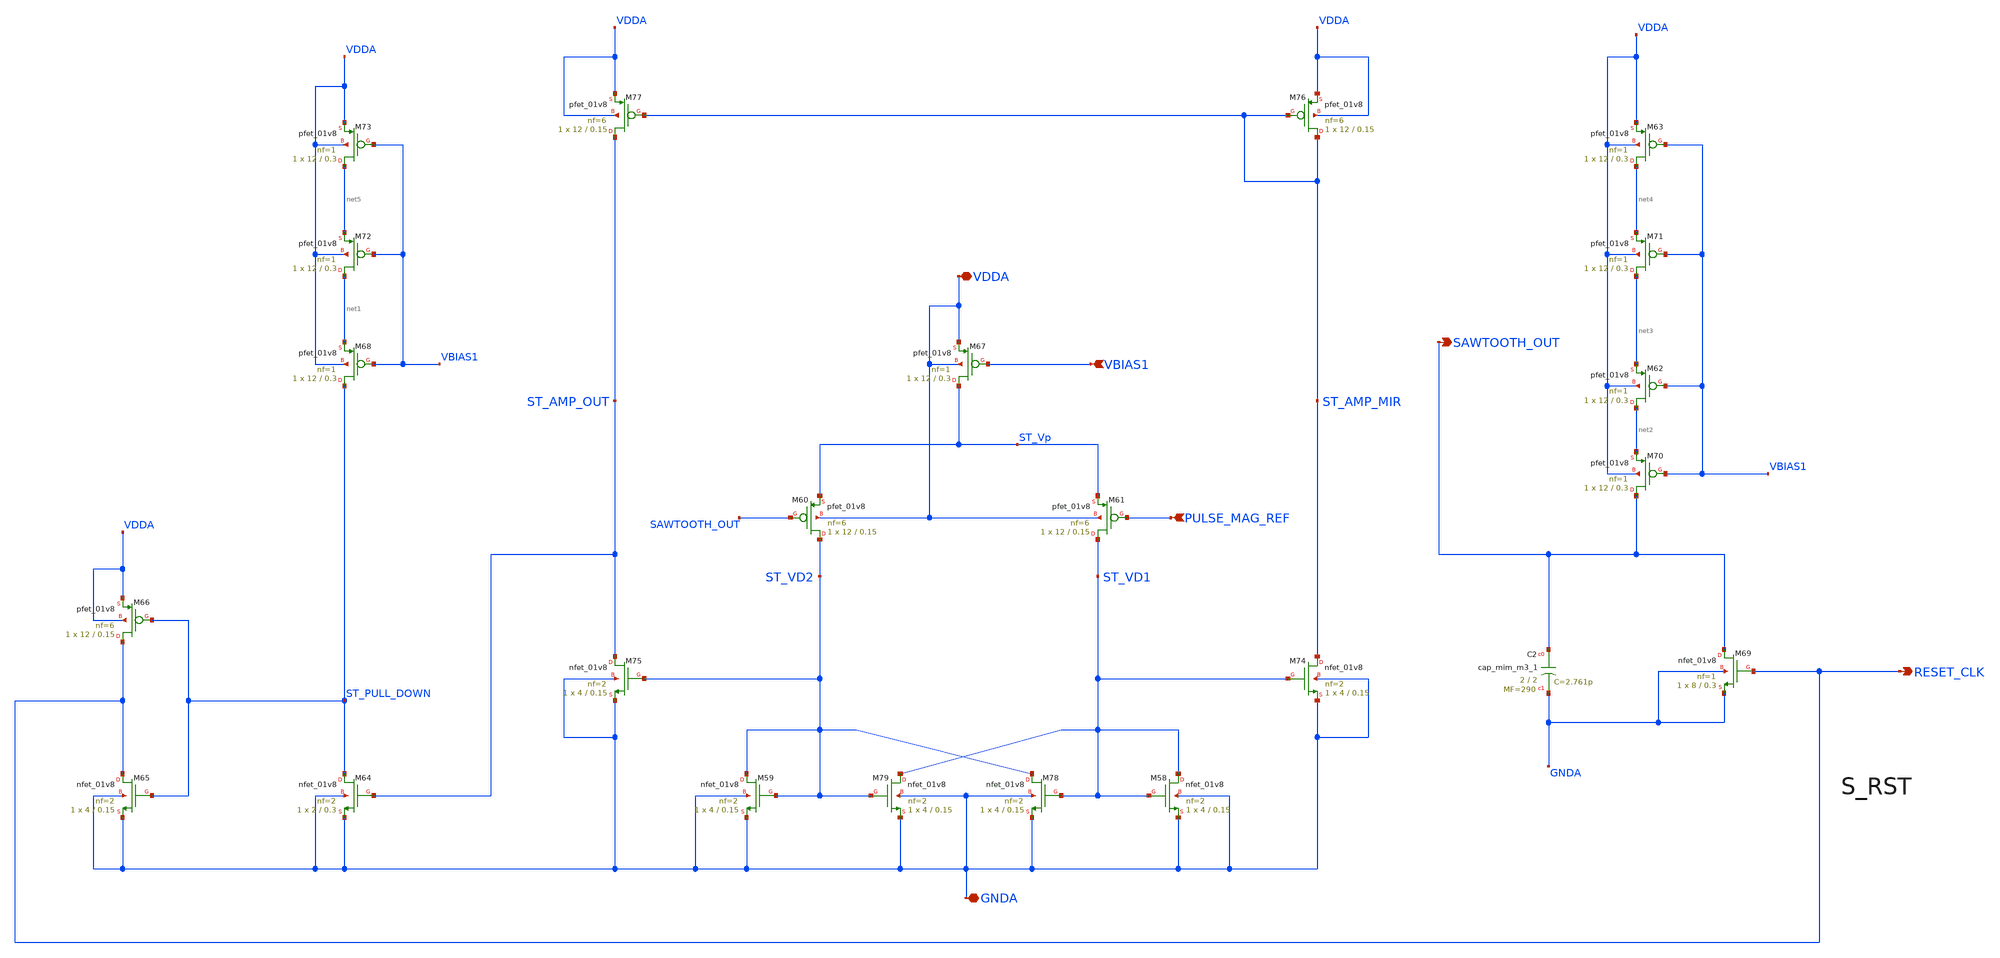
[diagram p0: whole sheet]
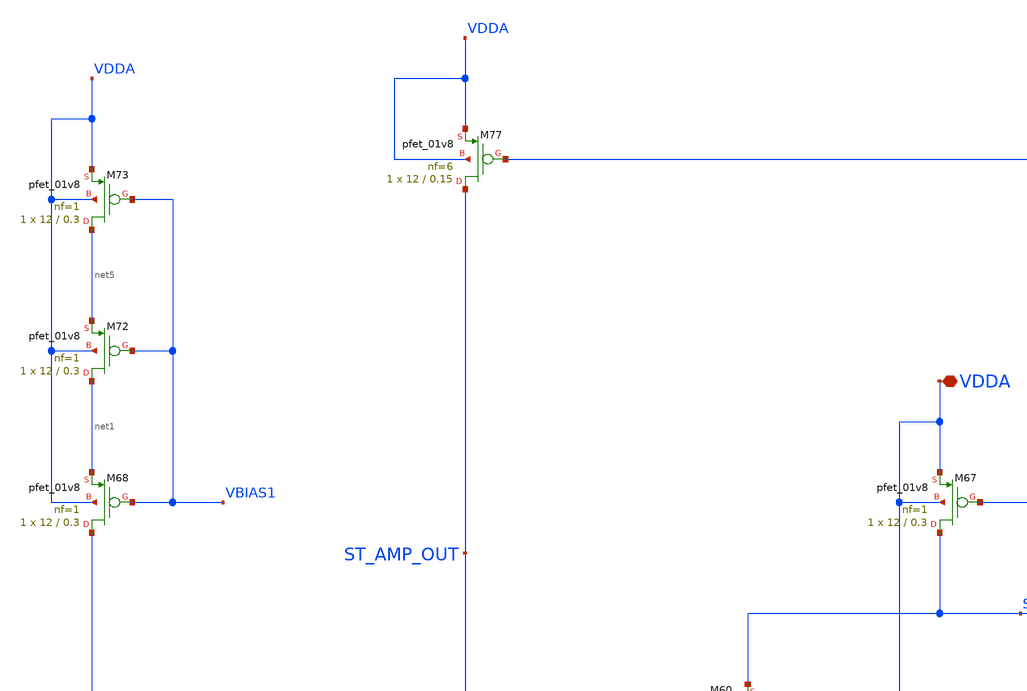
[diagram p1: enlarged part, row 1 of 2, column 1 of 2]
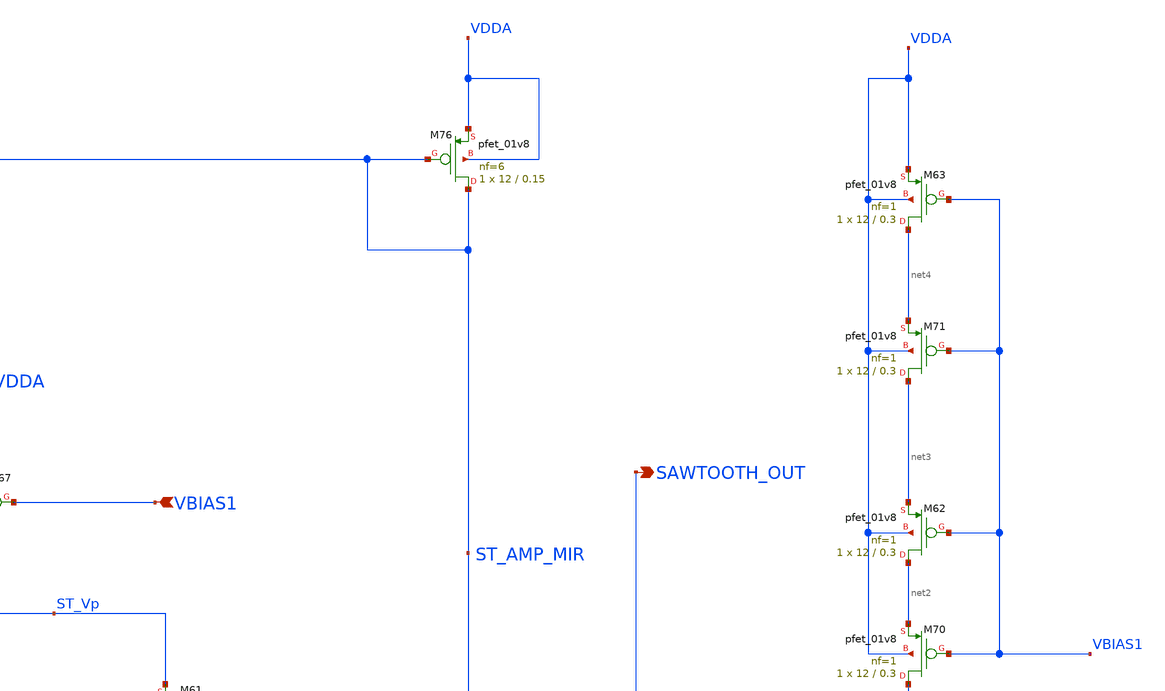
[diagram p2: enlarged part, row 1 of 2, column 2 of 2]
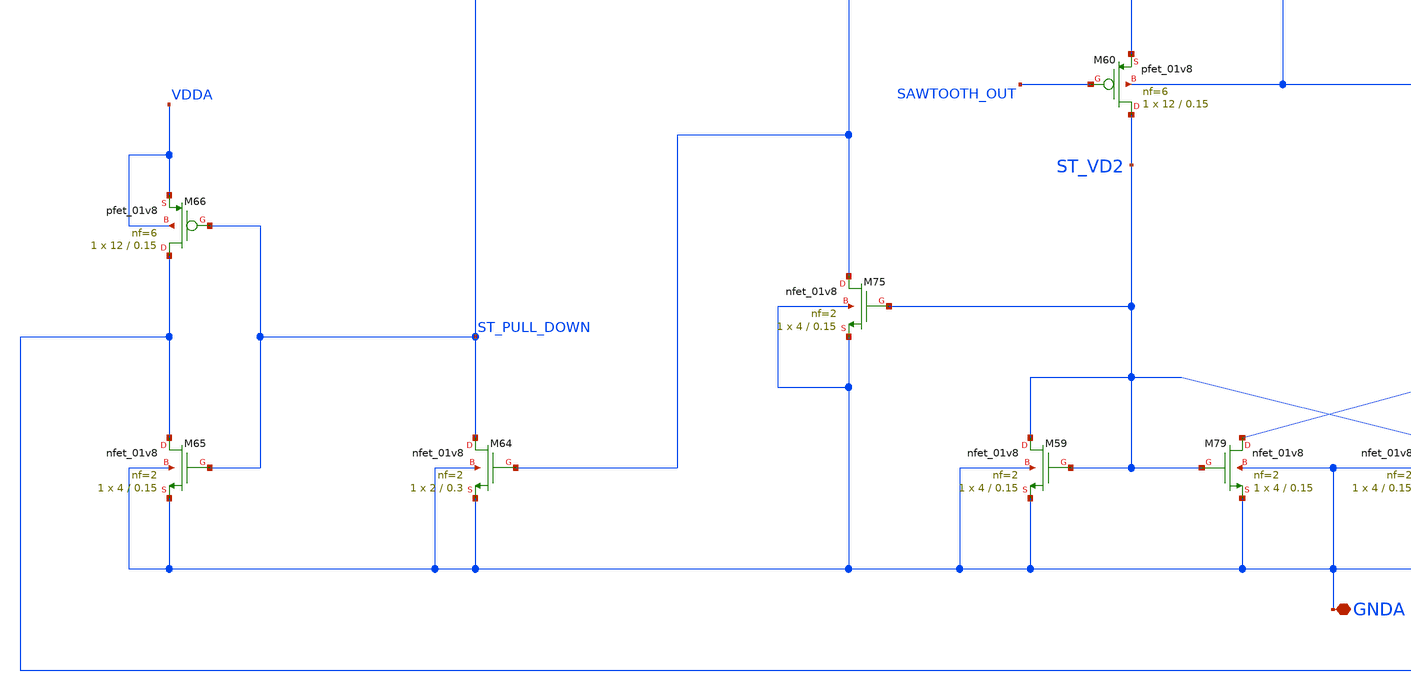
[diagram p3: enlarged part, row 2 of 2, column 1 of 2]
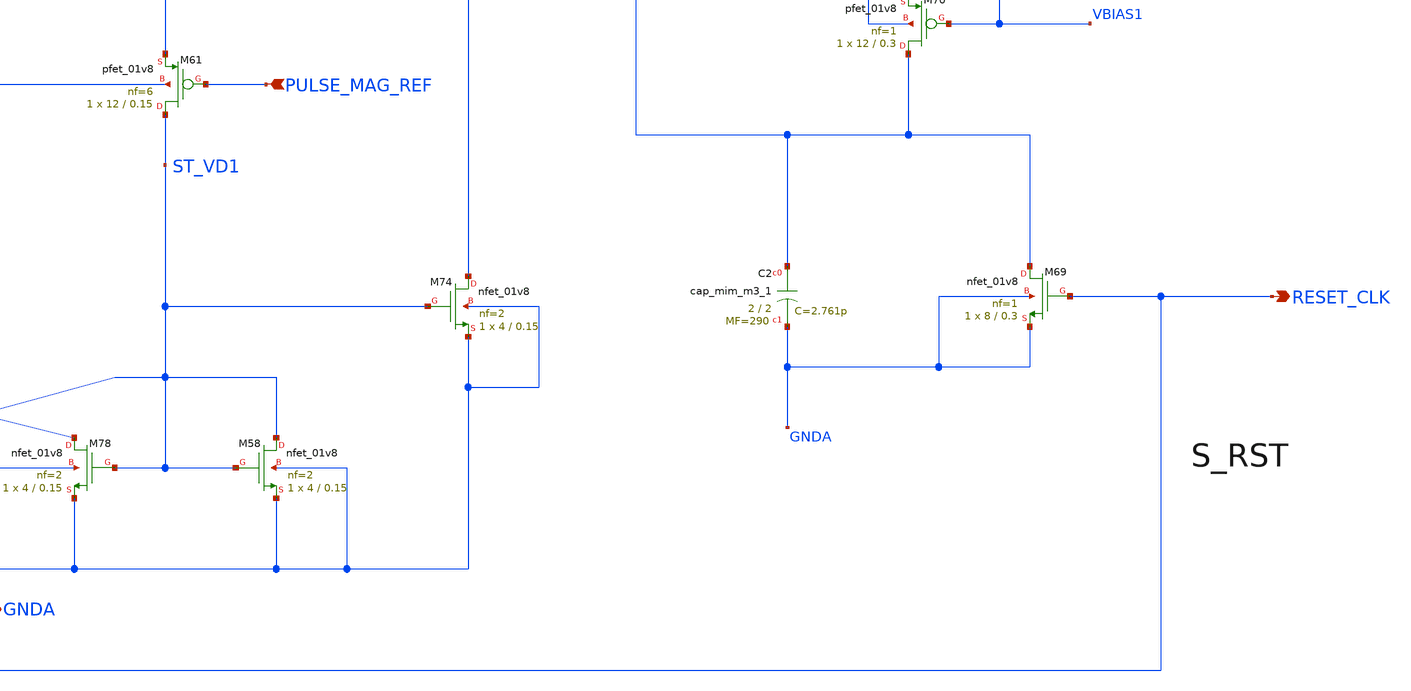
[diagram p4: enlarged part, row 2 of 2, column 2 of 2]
** sch_path: projects/ASU/EEE572/schematic/sawtooth_generator.sch
**.subckt sawtooth_generator VBIAS1 VDDA GNDA PULSE_MAG_REF SAWTOOTH_OUT RESET_CLK
*.ipin VBIAS1
*.iopin VDDA
*.iopin GNDA
*.ipin PULSE_MAG_REF
*.opin SAWTOOTH_OUT
*.opin RESET_CLK
XM58 ST_VD1 ST_VD1 GNDA GNDA sky130_fd_pr__nfet_01v8 L=0.15 W=4 nf=2 ad='int((nf+1)/2) * W/nf * 0.29'
+ as='int((nf+2)/2) * W/nf * 0.29' pd='2*int((nf+1)/2) * (W/nf + 0.29)' ps='2*int((nf+2)/2) * (W/nf + 0.29)'
+ nrd='0.29 / W' nrs='0.29 / W' sa=0 sb=0 sd=0 mult=1 m=1
XM59 ST_VD2 ST_VD2 GNDA GNDA sky130_fd_pr__nfet_01v8 L=0.15 W=4 nf=2 ad='int((nf+1)/2) * W/nf * 0.29'
+ as='int((nf+2)/2) * W/nf * 0.29' pd='2*int((nf+1)/2) * (W/nf + 0.29)' ps='2*int((nf+2)/2) * (W/nf + 0.29)'
+ nrd='0.29 / W' nrs='0.29 / W' sa=0 sb=0 sd=0 mult=1 m=1
XM60 ST_VD2 SAWTOOTH_OUT ST_Vp VDDA sky130_fd_pr__pfet_01v8 L=0.15 W=12 nf=6 ad='int((nf+1)/2) * W/nf * 0.29'
+ as='int((nf+2)/2) * W/nf * 0.29' pd='2*int((nf+1)/2) * (W/nf + 0.29)' ps='2*int((nf+2)/2) * (W/nf + 0.29)'
+ nrd='0.29 / W' nrs='0.29 / W' sa=0 sb=0 sd=0 mult=1 m=1
XM61 ST_VD1 PULSE_MAG_REF ST_Vp VDDA sky130_fd_pr__pfet_01v8 L=0.15 W=12 nf=6 ad='int((nf+1)/2) * W/nf * 0.29'
+ as='int((nf+2)/2) * W/nf * 0.29' pd='2*int((nf+1)/2) * (W/nf + 0.29)' ps='2*int((nf+2)/2) * (W/nf + 0.29)'
+ nrd='0.29 / W' nrs='0.29 / W' sa=0 sb=0 sd=0 mult=1 m=1
XM64 ST_PULL_DOWN ST_AMP_OUT GNDA GNDA sky130_fd_pr__nfet_01v8 L=0.3 W=2 nf=2 ad='int((nf+1)/2) * W/nf * 0.29'
+ as='int((nf+2)/2) * W/nf * 0.29' pd='2*int((nf+1)/2) * (W/nf + 0.29)' ps='2*int((nf+2)/2) * (W/nf + 0.29)'
+ nrd='0.29 / W' nrs='0.29 / W' sa=0 sb=0 sd=0 mult=1 m=1
XM65 RESET_CLK ST_PULL_DOWN GNDA GNDA sky130_fd_pr__nfet_01v8 L=0.15 W=4 nf=2 ad='int((nf+1)/2) * W/nf * 0.29'
+ as='int((nf+2)/2) * W/nf * 0.29' pd='2*int((nf+1)/2) * (W/nf + 0.29)' ps='2*int((nf+2)/2) * (W/nf + 0.29)'
+ nrd='0.29 / W' nrs='0.29 / W' sa=0 sb=0 sd=0 mult=1 m=1
XM66 RESET_CLK ST_PULL_DOWN VDDA VDDA sky130_fd_pr__pfet_01v8 L=0.15 W=12 nf=6 ad='int((nf+1)/2) * W/nf * 0.29'
+ as='int((nf+2)/2) * W/nf * 0.29' pd='2*int((nf+1)/2) * (W/nf + 0.29)' ps='2*int((nf+2)/2) * (W/nf + 0.29)'
+ nrd='0.29 / W' nrs='0.29 / W' sa=0 sb=0 sd=0 mult=1 m=1
XM67 ST_Vp VBIAS1 VDDA VDDA sky130_fd_pr__pfet_01v8 L=0.3 W=12 nf=1 ad='int((nf+1)/2) * W/nf * 0.29'
+ as='int((nf+2)/2) * W/nf * 0.29' pd='2*int((nf+1)/2) * (W/nf + 0.29)' ps='2*int((nf+2)/2) * (W/nf + 0.29)'
+ nrd='0.29 / W' nrs='0.29 / W' sa=0 sb=0 sd=0 mult=1 m=1
XM68 ST_PULL_DOWN VBIAS1 net1 VDDA sky130_fd_pr__pfet_01v8 L=0.3 W=12 nf=1 ad='int((nf+1)/2) * W/nf * 0.29'
+ as='int((nf+2)/2) * W/nf * 0.29' pd='2*int((nf+1)/2) * (W/nf + 0.29)' ps='2*int((nf+2)/2) * (W/nf + 0.29)'
+ nrd='0.29 / W' nrs='0.29 / W' sa=0 sb=0 sd=0 mult=1 m=1
XC2 SAWTOOTH_OUT GNDA sky130_fd_pr__cap_mim_m3_1 W=2 L=2 MF=290 m=290
XM69 SAWTOOTH_OUT RESET_CLK GNDA GNDA sky130_fd_pr__nfet_01v8 L=0.3 W=8 nf=1 ad='int((nf+1)/2) * W/nf * 0.29'
+ as='int((nf+2)/2) * W/nf * 0.29' pd='2*int((nf+1)/2) * (W/nf + 0.29)' ps='2*int((nf+2)/2) * (W/nf + 0.29)'
+ nrd='0.29 / W' nrs='0.29 / W' sa=0 sb=0 sd=0 mult=1 m=1
XM70 SAWTOOTH_OUT VBIAS1 net2 VDDA sky130_fd_pr__pfet_01v8 L=0.3 W=12 nf=1 ad='int((nf+1)/2) * W/nf * 0.29'
+ as='int((nf+2)/2) * W/nf * 0.29' pd='2*int((nf+1)/2) * (W/nf + 0.29)' ps='2*int((nf+2)/2) * (W/nf + 0.29)'
+ nrd='0.29 / W' nrs='0.29 / W' sa=0 sb=0 sd=0 mult=1 m=1
XM62 net2 VBIAS1 net3 VDDA sky130_fd_pr__pfet_01v8 L=0.3 W=12 nf=1 ad='int((nf+1)/2) * W/nf * 0.29' as='int((nf+2)/2) * W/nf * 0.29'
+ pd='2*int((nf+1)/2) * (W/nf + 0.29)' ps='2*int((nf+2)/2) * (W/nf + 0.29)' nrd='0.29 / W' nrs='0.29 / W'
+ sa=0 sb=0 sd=0 mult=1 m=1
XM63 net4 VBIAS1 VDDA VDDA sky130_fd_pr__pfet_01v8 L=0.3 W=12 nf=1 ad='int((nf+1)/2) * W/nf * 0.29' as='int((nf+2)/2) * W/nf * 0.29'
+ pd='2*int((nf+1)/2) * (W/nf + 0.29)' ps='2*int((nf+2)/2) * (W/nf + 0.29)' nrd='0.29 / W' nrs='0.29 / W'
+ sa=0 sb=0 sd=0 mult=1 m=1
XM71 net3 VBIAS1 net4 VDDA sky130_fd_pr__pfet_01v8 L=0.3 W=12 nf=1 ad='int((nf+1)/2) * W/nf * 0.29' as='int((nf+2)/2) * W/nf * 0.29'
+ pd='2*int((nf+1)/2) * (W/nf + 0.29)' ps='2*int((nf+2)/2) * (W/nf + 0.29)' nrd='0.29 / W' nrs='0.29 / W'
+ sa=0 sb=0 sd=0 mult=1 m=1
XM72 net1 VBIAS1 net5 VDDA sky130_fd_pr__pfet_01v8 L=0.3 W=12 nf=1 ad='int((nf+1)/2) * W/nf * 0.29' as='int((nf+2)/2) * W/nf * 0.29'
+ pd='2*int((nf+1)/2) * (W/nf + 0.29)' ps='2*int((nf+2)/2) * (W/nf + 0.29)' nrd='0.29 / W' nrs='0.29 / W'
+ sa=0 sb=0 sd=0 mult=1 m=1
XM73 net5 VBIAS1 VDDA VDDA sky130_fd_pr__pfet_01v8 L=0.3 W=12 nf=1 ad='int((nf+1)/2) * W/nf * 0.29' as='int((nf+2)/2) * W/nf * 0.29'
+ pd='2*int((nf+1)/2) * (W/nf + 0.29)' ps='2*int((nf+2)/2) * (W/nf + 0.29)' nrd='0.29 / W' nrs='0.29 / W'
+ sa=0 sb=0 sd=0 mult=1 m=1
XM74 ST_AMP_MIR ST_VD1 GNDA GNDA sky130_fd_pr__nfet_01v8 L=0.15 W=4 nf=2 ad='int((nf+1)/2) * W/nf * 0.29'
+ as='int((nf+2)/2) * W/nf * 0.29' pd='2*int((nf+1)/2) * (W/nf + 0.29)' ps='2*int((nf+2)/2) * (W/nf + 0.29)'
+ nrd='0.29 / W' nrs='0.29 / W' sa=0 sb=0 sd=0 mult=1 m=1
XM75 ST_AMP_OUT ST_VD2 GNDA GNDA sky130_fd_pr__nfet_01v8 L=0.15 W=4 nf=2 ad='int((nf+1)/2) * W/nf * 0.29'
+ as='int((nf+2)/2) * W/nf * 0.29' pd='2*int((nf+1)/2) * (W/nf + 0.29)' ps='2*int((nf+2)/2) * (W/nf + 0.29)'
+ nrd='0.29 / W' nrs='0.29 / W' sa=0 sb=0 sd=0 mult=1 m=1
XM76 ST_AMP_MIR ST_AMP_MIR VDDA VDDA sky130_fd_pr__pfet_01v8 L=0.15 W=12 nf=6 ad='int((nf+1)/2) * W/nf * 0.29'
+ as='int((nf+2)/2) * W/nf * 0.29' pd='2*int((nf+1)/2) * (W/nf + 0.29)' ps='2*int((nf+2)/2) * (W/nf + 0.29)'
+ nrd='0.29 / W' nrs='0.29 / W' sa=0 sb=0 sd=0 mult=1 m=1
XM77 ST_AMP_OUT ST_AMP_MIR VDDA VDDA sky130_fd_pr__pfet_01v8 L=0.15 W=12 nf=6 ad='int((nf+1)/2) * W/nf * 0.29'
+ as='int((nf+2)/2) * W/nf * 0.29' pd='2*int((nf+1)/2) * (W/nf + 0.29)' ps='2*int((nf+2)/2) * (W/nf + 0.29)'
+ nrd='0.29 / W' nrs='0.29 / W' sa=0 sb=0 sd=0 mult=1 m=1
XM78 ST_VD2 ST_VD1 GNDA GNDA sky130_fd_pr__nfet_01v8 L=0.15 W=4 nf=2 ad='int((nf+1)/2) * W/nf * 0.29'
+ as='int((nf+2)/2) * W/nf * 0.29' pd='2*int((nf+1)/2) * (W/nf + 0.29)' ps='2*int((nf+2)/2) * (W/nf + 0.29)'
+ nrd='0.29 / W' nrs='0.29 / W' sa=0 sb=0 sd=0 mult=1 m=1
XM79 ST_VD1 ST_VD2 GNDA GNDA sky130_fd_pr__nfet_01v8 L=0.15 W=4 nf=2 ad='int((nf+1)/2) * W/nf * 0.29'
+ as='int((nf+2)/2) * W/nf * 0.29' pd='2*int((nf+1)/2) * (W/nf + 0.29)' ps='2*int((nf+2)/2) * (W/nf + 0.29)'
+ nrd='0.29 / W' nrs='0.29 / W' sa=0 sb=0 sd=0 mult=1 m=1
**.ends
.end
